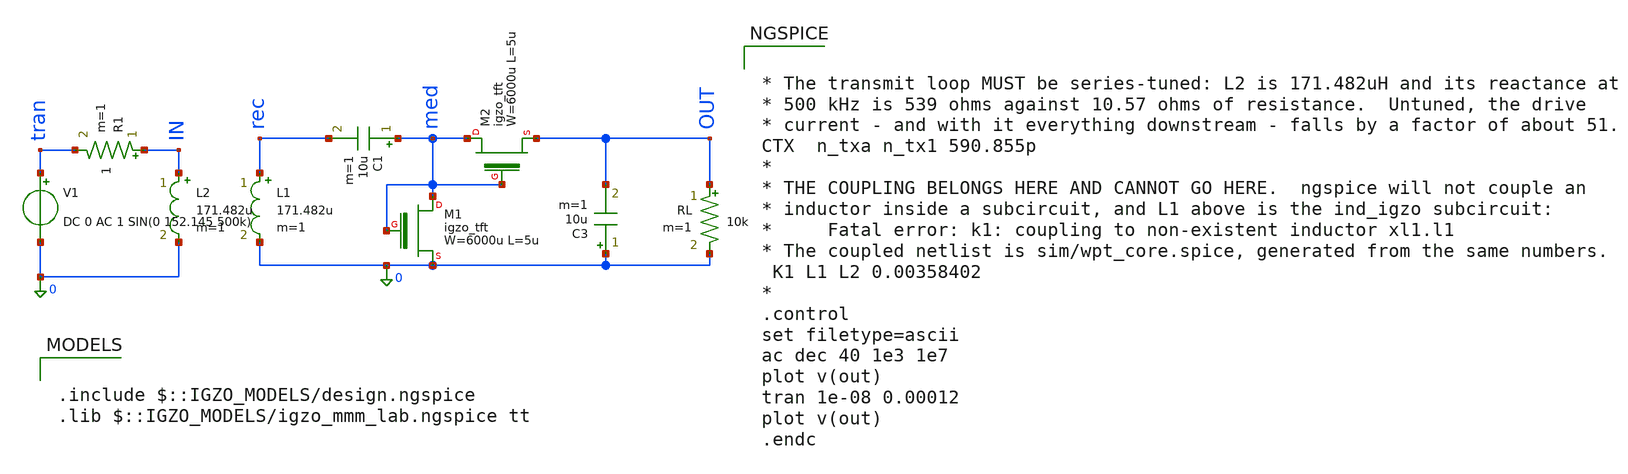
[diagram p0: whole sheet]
** sch_path: WPT/WPT.sch
**.subckt WPT
C1 med rec 10u m=1
XM1 med med 0 igzo_tft W=6000u L=5u ov=2u nf=1 m=1
XM2 med med OUT igzo_tft W=6000u L=5u ov=2u nf=1 m=1
C3 0 OUT 10u m=1
RL OUT 0 10k m=1
V1 tran 0 DC 0 AC 1 SIN(0 152.145 500k)
.save i(v1)
R1 IN tran 1 m=1
L2 IN 0 171.482u m=1
L1 rec 0 171.482u m=1
**** begin user architecture code

.include $::IGZO_MODELS/design.ngspice
.lib $::IGZO_MODELS/igzo_mmm_lab.ngspice tt



* The transmit loop MUST be series-tuned: L2 is 171.482uH and its reactance at
* 500 kHz is 539 ohms against 10.57 ohms of resistance.  Untuned, the drive
* current - and with it everything downstream - falls by a factor of about 51.
CTX  n_txa n_tx1 590.855p
*
* THE COUPLING BELONGS HERE AND CANNOT GO HERE.  ngspice will not couple an
* inductor inside a subcircuit, and L1 above is the ind_igzo subcircuit:
*     Fatal error: k1: coupling to non-existent inductor xl1.l1
* The coupled netlist is sim/wpt_core.spice, generated from the same numbers.
 K1 L1 L2 0.00358402
*
.control
set filetype=ascii
ac dec 40 1e3 1e7
plot v(out)
tran 1e-08 0.00012
plot v(out)
.endc


**** end user architecture code
**.ends
.end
